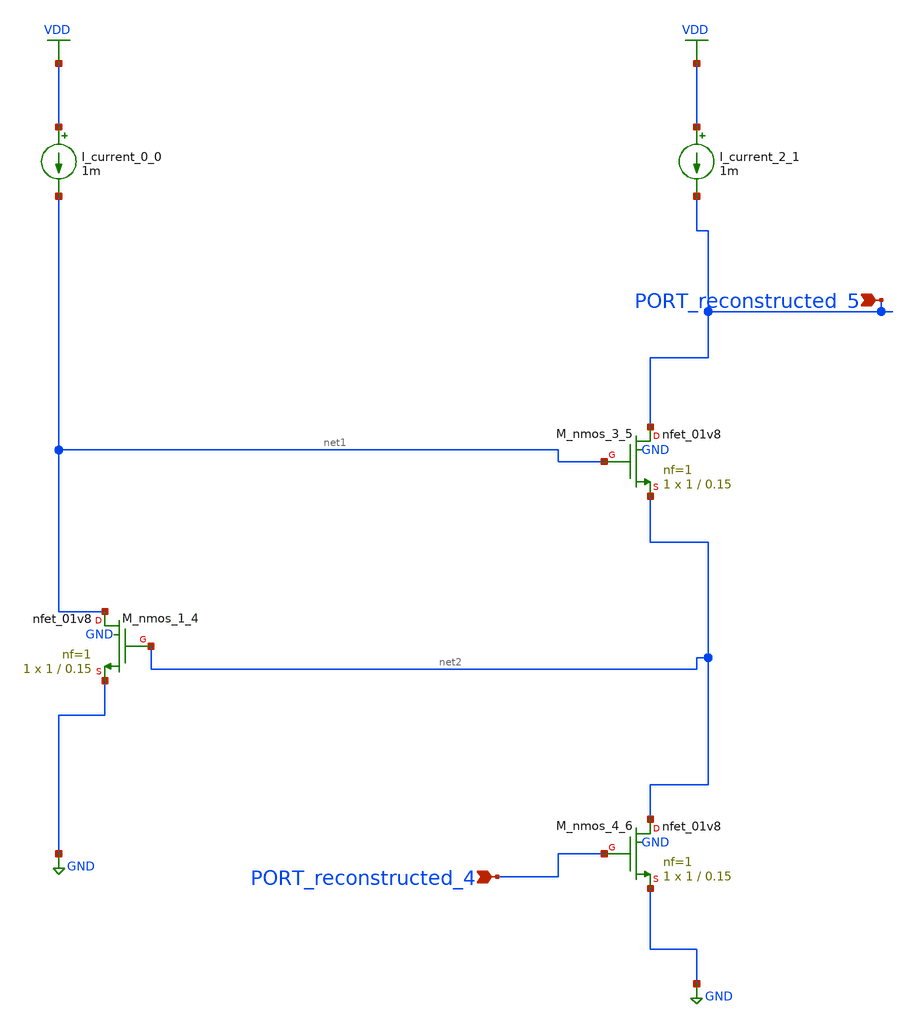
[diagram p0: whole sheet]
** sch_path: schematics/AMSNet/651.sch
**.subckt 651 PORT_reconstructed_4 PORT_reconstructed_5
*.ipin PORT_reconstructed_4
*.ipin PORT_reconstructed_5
I_current_0_0 VDD net1 1m
I_current_2_1 VDD PORT_reconstructed_5 1m
XM_nmos_1_4 net1 net2 GND GND sky130_fd_pr__nfet_01v8 L=0.15 W=1 nf=1 ad='int((1 + 1)/2) * 1 / 1 * 0.29'
+ as='int((1 + 2)/2) * 1 / 1 * 0.29' pd='2*int((1 + 1)/2) * (1 / 1 + 0.29)' ps='2*int((1 + 2)/2) * (1 / 1 + 0.29)'
+ nrd='0.29 / 1 ' nrs='0.29 / 1 ' sa=0 sb=0 sd=0 mult=1 m=1
XM_nmos_3_5 PORT_reconstructed_5 net1 net2 GND sky130_fd_pr__nfet_01v8 L=0.15 W=1 nf=1 ad='int((1 + 1)/2) * 1 / 1 * 0.29'
+ as='int((1 + 2)/2) * 1 / 1 * 0.29' pd='2*int((1 + 1)/2) * (1 / 1 + 0.29)' ps='2*int((1 + 2)/2) * (1 / 1 + 0.29)'
+ nrd='0.29 / 1 ' nrs='0.29 / 1 ' sa=0 sb=0 sd=0 mult=1 m=1
XM_nmos_4_6 net2 PORT_reconstructed_4 GND GND sky130_fd_pr__nfet_01v8 L=0.15 W=1 nf=1 ad='int((1 + 1)/2) * 1 / 1 * 0.29'
+ as='int((1 + 2)/2) * 1 / 1 * 0.29' pd='2*int((1 + 1)/2) * (1 / 1 + 0.29)' ps='2*int((1 + 2)/2) * (1 / 1 + 0.29)'
+ nrd='0.29 / 1 ' nrs='0.29 / 1 ' sa=0 sb=0 sd=0 mult=1 m=1
**.ends
.GLOBAL GND
.GLOBAL VDD
.end
